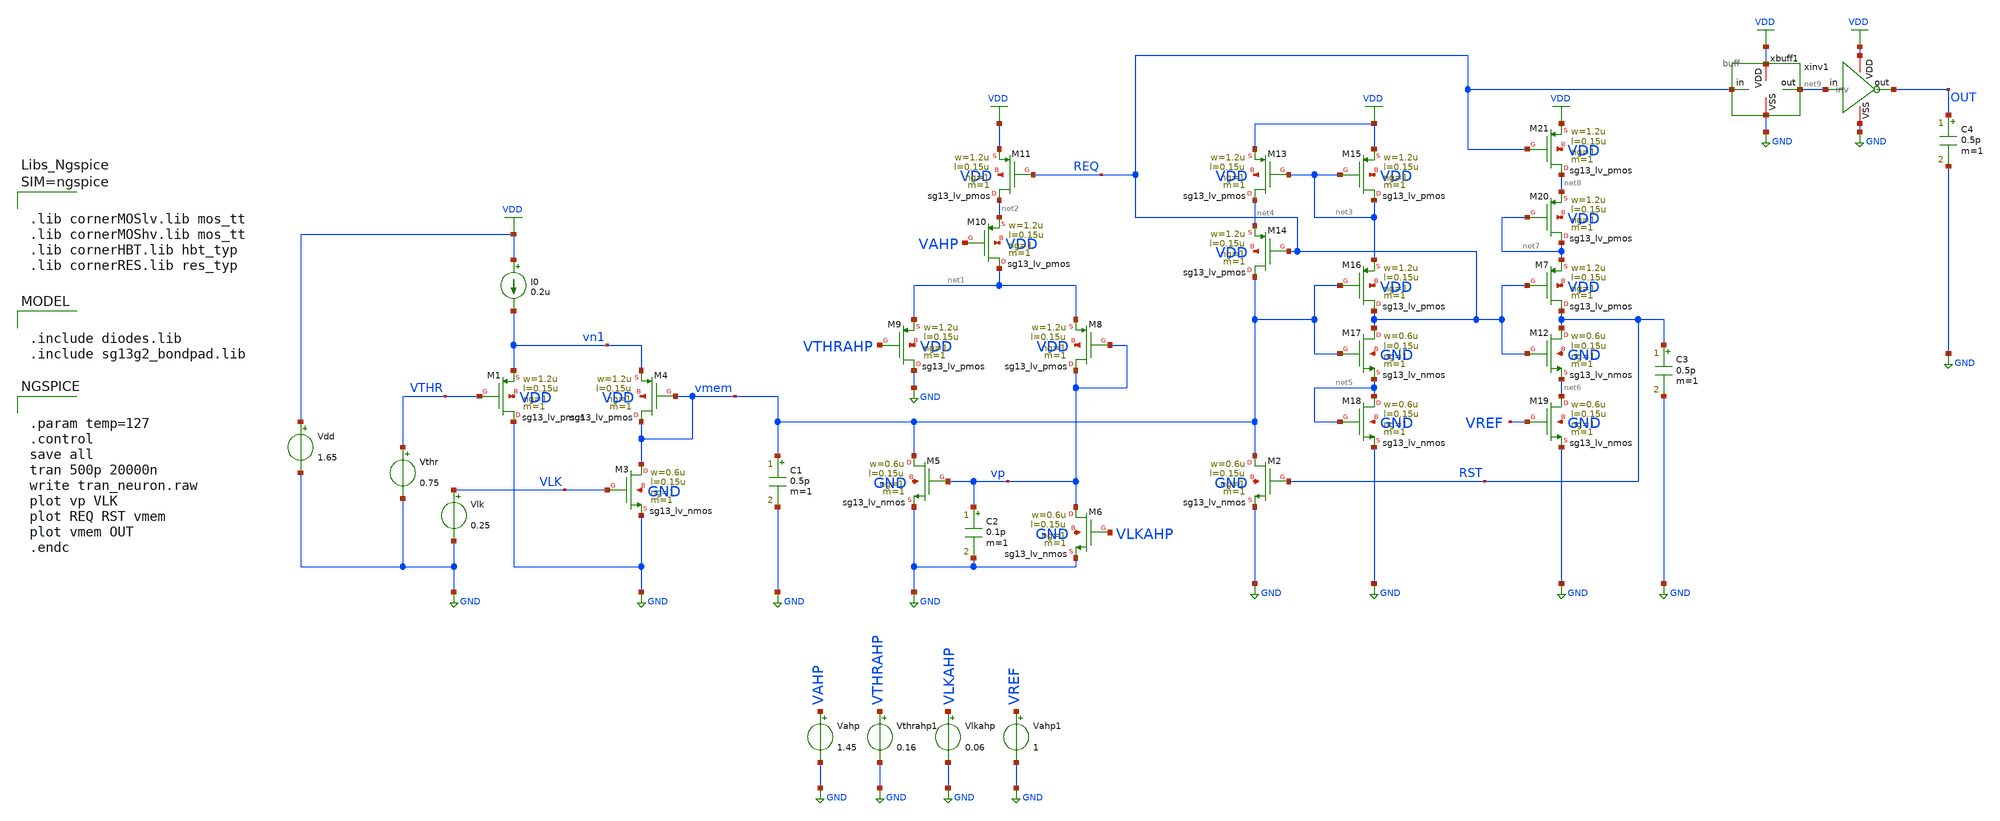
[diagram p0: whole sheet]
** sch_path: blocks/composite/dpi_adexp_neuron/design_data/xschem/neuron_buff_test.sch
**.subckt neuron_buff_test
I0 VDD vn1 0.2u
XM3 vmem VLK GND GND sg13_lv_nmos w=0.6u l=0.15u ng=1 m=1 mm_ok=1
XM1 GND VTHR vn1 VDD sg13_lv_pmos w=1.2u l=0.15u ng=1 m=1 mm_ok=1
XM4 vmem vmem vn1 VDD sg13_lv_pmos w=1.2u l=0.15u ng=1 m=1 mm_ok=1
C1 vmem GND 0.5p m=1
Vdd VDD GND 1.65
Vlk VLK GND 0.25
Vthr VTHR GND 0.75
XM2 vmem RST GND GND sg13_lv_nmos w=0.6u l=0.15u ng=1 m=1 mm_ok=1
XM5 vmem vp GND GND sg13_lv_nmos w=0.6u l=0.15u ng=1 m=1 mm_ok=1
C2 vp GND 0.1p m=1
XM6 vp VLKAHP GND GND sg13_lv_nmos w=0.6u l=0.15u ng=1 m=1 mm_ok=1
XM8 vp vp net1 VDD sg13_lv_pmos w=1.2u l=0.15u ng=1 m=1 mm_ok=1
XM9 GND VTHRAHP net1 VDD sg13_lv_pmos w=1.2u l=0.15u ng=1 m=1 mm_ok=1
XM10 net1 VAHP net2 VDD sg13_lv_pmos w=1.2u l=0.15u ng=1 m=1 mm_ok=1
XM11 net2 REQ VDD VDD sg13_lv_pmos w=1.2u l=0.15u ng=1 m=1 mm_ok=1
XM13 net4 net3 VDD VDD sg13_lv_pmos w=1.2u l=0.15u ng=1 m=1 mm_ok=1
XM14 vmem REQ net4 VDD sg13_lv_pmos w=1.2u l=0.15u ng=1 m=1 mm_ok=1
XM15 net3 net3 VDD VDD sg13_lv_pmos w=1.2u l=0.15u ng=1 m=1 mm_ok=1
XM16 REQ vmem net3 VDD sg13_lv_pmos w=1.2u l=0.15u ng=1 m=1 mm_ok=1
XM17 REQ vmem net5 GND sg13_lv_nmos w=0.6u l=0.15u ng=1 m=1 mm_ok=1
XM18 net5 net5 GND GND sg13_lv_nmos w=0.6u l=0.15u ng=1 m=1 mm_ok=1
Vlkahp VLKAHP GND 0.06
Vthrahp1 VTHRAHP GND 0.16
Vahp VAHP GND 1.45
XM7 RST REQ net7 VDD sg13_lv_pmos w=1.2u l=0.15u ng=1 m=1 mm_ok=1
XM12 RST REQ net6 GND sg13_lv_nmos w=0.6u l=0.15u ng=1 m=1 mm_ok=1
XM19 net6 VREF GND GND sg13_lv_nmos w=0.6u l=0.15u ng=1 m=1 mm_ok=1
C3 RST GND 0.5p m=1
XM20 net7 net7 net8 VDD sg13_lv_pmos w=1.2u l=0.15u ng=1 m=1 mm_ok=1
XM21 net8 REQ VDD VDD sg13_lv_pmos w=1.2u l=0.15u ng=1 m=1 mm_ok=1
Vahp1 VREF GND 1
xbuff1 VDD REQ net9 GND buff
C4 OUT GND 0.5p m=1
xinv1 VDD net9 OUT GND inv
**** begin user architecture code

.include diodes.lib
.include sg13g2_bondpad.lib



.param temp=127
.control
save all
tran 500p 20000n
write tran_neuron.raw
plot vp VLK
plot REQ RST vmem
plot vmem OUT
.endc





.lib cornerMOSlv.lib mos_tt
.lib cornerMOShv.lib mos_tt
.lib cornerHBT.lib hbt_typ
.lib cornerRES.lib res_typ



**** end user architecture code
**.ends
.GLOBAL GND
.GLOBAL VDD
.end
